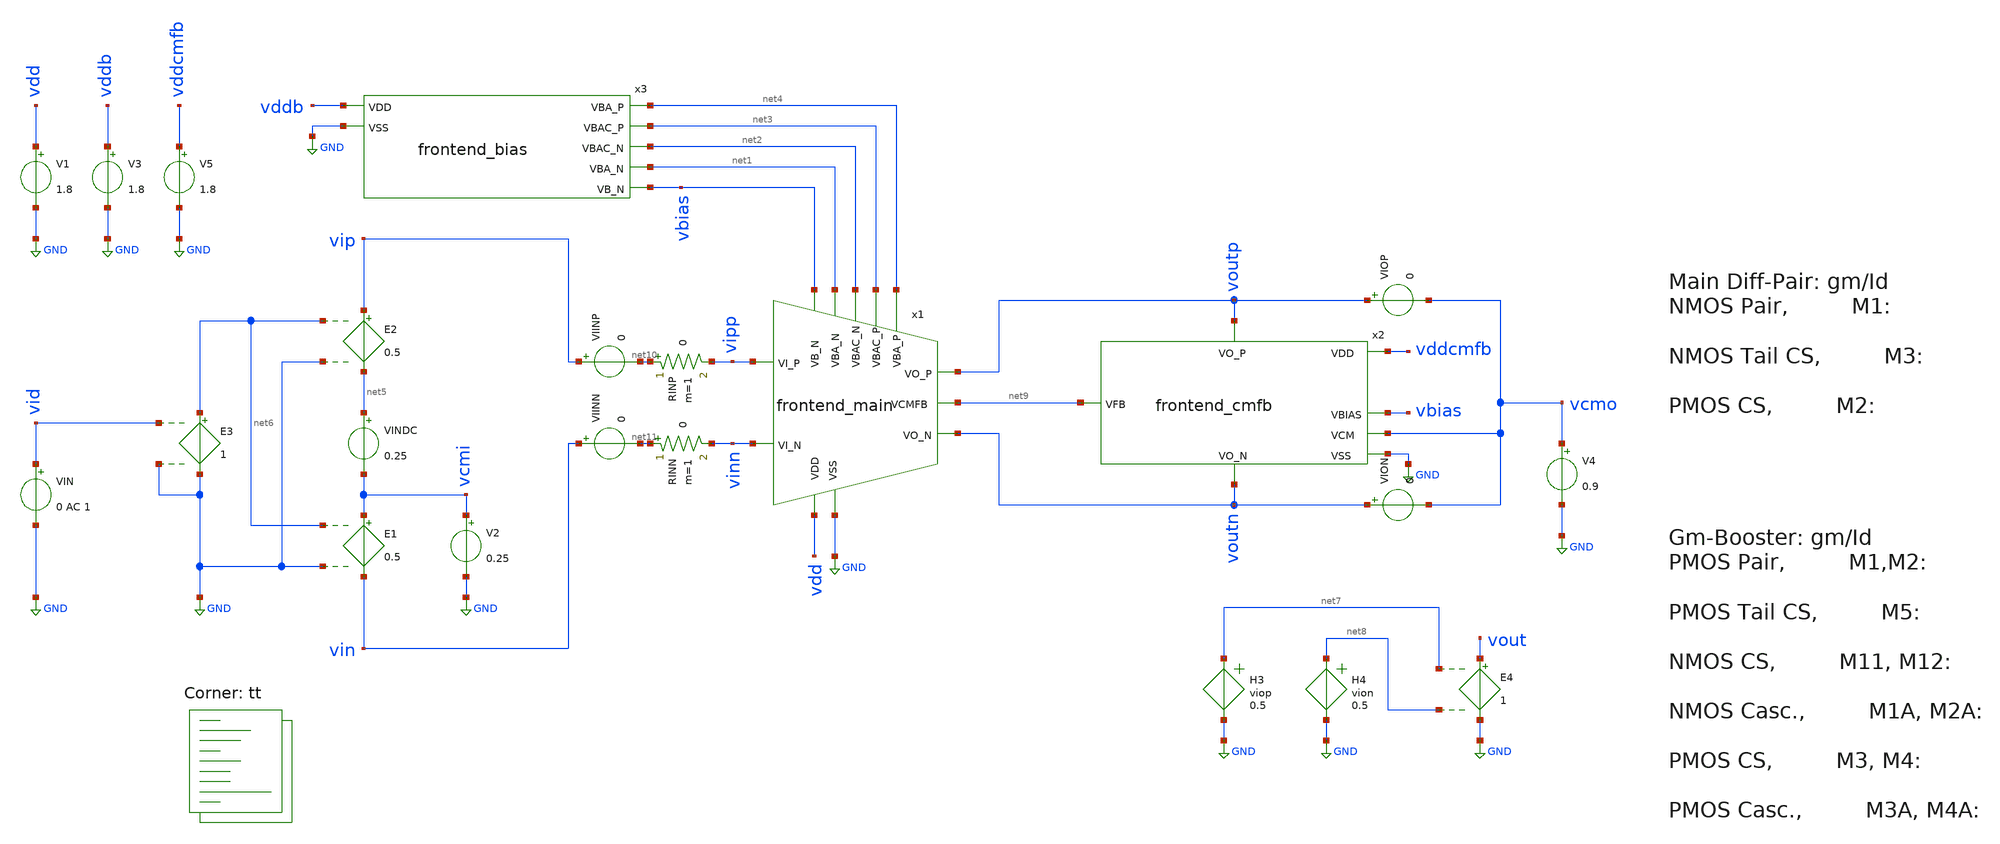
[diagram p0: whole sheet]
** sch_path: circuit-level/xschem/frontend/frontend_tb_dc.sch
**.subckt frontend_tb_dc
V1 vdd GND 1.8
V2 vcmi GND 0.25
E1 vcmi vin net6 GND 0.5
E2 vip net5 net6 GND 0.5
VIN vid GND 0 AC 1
VINDC net5 vcmi 0.25
x2 vddcmfb net9 voutp voutn vbias vcmo GND frontend_cmfb
x3 vddb net4 net3 net2 net1 vbias GND frontend_bias
V3 vddb GND 1.8
V4 vcmo GND 0.9
E3 net6 GND vid GND 1
VIOP voutp vcmo 0
VION voutn vcmo 0
H3 net7 GND viop 0.5
H4 net8 GND vion 0.5
E4 vout GND net7 net8 1
x1 vdd net9 net1 net2 net3 net4 voutp voutn vipp vinn vbias GND frontend_main
V5 vddcmfb GND 1.8
RINP net10 vipp 0 m=1
RINN net11 vinn 0 m=1
VIINP vip net10 0
VIINN vin net11 0
**** begin user architecture code
.lib $::SKYWATER_MODELS/sky130.lib.spice tt


.options savecurrents
.control
save all

let f_sig = 32
let f_min = 0.1
let f_max = 128
let tper_sig = 1/f_sig
let tfr_sig = tper_sig/2
alter @VIN[SIN] = [ 0 0.01 $&f_sig 0 0 0 ]
alter @VIN[DC] = 0.0

let tstep = 0.01/f_sig
let tstop = 500/f_sig
let tstart = 2500*tstep

set fndc = /foss/designs/frontend/frontend_dc.txt
set fntran = /foss/designs/frontend/frontend_tran.txt
set fnspec = /foss/designs/frontend/frontend_spec.txt
set fnhd = /foss/designs/frontend/frontend_hd.txt
set fnnoise = /foss/designs/frontend/frontend_noise.txt
set wr_singlescale
set wr_vecnames
option numdgt=5


** Main Simulations
	alter @VINDC[DC] = 0
	dc VIN -500m 500m 31m
	ac dec 1000 0.1 1e7
	alter @VINDC[DC] = 0.25
	tran $&tstep $&tstop $&tstart
	alter @VINDC[DC] = 0
	noise v(vout) VIN dec 100 0.01 100k 1
	noise v(vout) VIN dec 10 0.01 128
	alter @rinp[resistance] = 10G
	alter @rinn[resistance] = 10G
	alter @VIN[SIN] = [ 0 0.1 128 0 0 0 ]
	alter @VINDC[DC] = 0
	tran $&tstep $&tstop $&tstart

	setplot noise1
	let acgain = onoise_spectrum/inoise_spectrum

	let mdiffpair_gmb_in = sqrt(4)*onoise.m.x1.x1.xm1a.msky130_fd_pr__pfet_01v8/acgain
	let mload_gmb_in = sqrt(4)*onoise.m.x1.x1.xm3a.msky130_fd_pr__nfet_01v8/acgain
	let mload_in = sqrt(2)*onoise.m.x1.xm2a.msky130_fd_pr__pfet_01v8_lvt/acgain
	let mdiffpair_in = sqrt(2)*onoise.m.x1.xm1a.msky130_fd_pr__nfet_01v8/acgain
	let mtail_in = onoise.m.x1.xm3a.msky130_fd_pr__nfet_01v8/acgain
	*let m1b_in = onoise.m.xm1b.msky130_fd_pr__nfet_01v8/acgain

	*let m2a_in = onoise.m.xm2a.msky130_fd_pr__pfet_01v8_lvt/acgain
	*let m2b_in = onoise.m.xm2b.msky130_fd_pr__pfet_01v8_lvt/acgain

	*let m3a_in = onoise.m.xm3a.msky130_fd_pr__nfet_01v8/acgain
	*let m3b_in = onoise.m.xm3b.msky130_fd_pr__nfet_01v8/acgain

	let rs_in = sqrt(onoise_r.x1.rs1^2+onoise_r.x1.rs2^2)/acgain

	*plot inoise_spectrum m1a_in m2a_in m3a_in rs_in

	*plot m2a_in m2b_in
	plot inoise_spectrum rs_in mdiffpair_gmb_in mload_gmb_in mload_in mdiffpair_in ylog xlog
	wrdata $fnnoise inoise_spectrum rs_in mdiffpair_gmb_in mload_gmb_in mload_in mdiffpair_in

	setplot ac1
	let A = v(vout)/v(vin)
	plot vdb(A) 180/PI*phase(A)

	let i_in_p = viinp#branch
	let i_in_n = viinn#branch
	let zin = abs((v(vip)-v(vin))/(2*(i_in_p-i_in_n)))
	meas ac zin_fmax find zin when frequency=128

	plot vdb(zin)

	setplot dc1
	let vid = v(vid)
	let iod = (viop#branch-vion#branch)
	let gm  = abs(iod/vid)
	plot iod
	plot gm 0
	wrdata $fndc iod gm

	setplot tran1
	let vid = v(vid)
	let iod = (viop#branch-vion#branch)

	meas tran iod_max max iod
	meas tran vid_max max vid
	let gm = iod_max/vid_max
	plot iod

	*plot gm
	wrdata $fntran iod

	** FFT

	linearize iod
	set specwindow=hanning
	fft iod
	setplot sp5

	let N = length(iod)
	let fres = frequency[n-1]/n
	let fmin_idx = ceil(const.f_min/fres)
	let fmax_idx = ceil(const.f_max/fres)

	let iod_spec = mag(iod)
	let iod_spec_slice = iod_spec[fmin_idx,fmax_idx]
	let freq = frequency[fmin_idx,fmax_idx]
	meas sp iod_max max iod_spec_slice
	let iod_spec_db = 20*log10(iod_spec_slice/iod_max)
	plot iod_spec_db vs freq

	** Calc HD2, HD3
	let sig_idx = ceil(const.f_sig/fres)
	let hd2_idx = 2*sig_idx
	let hd3_idx = 3*sig_idx
	let sig_pwr = iod_spec[sig_idx-1]^2+iod_spec[sig_idx]^2+iod_spec[sig_idx+1]^2
	let hd2_pwr = iod_spec[hd2_idx-1]^2+iod_spec[hd2_idx]^2+iod_spec[hd2_idx+1]^2
	let hd3_pwr = iod_spec[hd3_idx-1]^2+iod_spec[hd3_idx]^2+iod_spec[hd3_idx+1]^2
	let hd2 = sqrt(hd2_pwr/sig_pwr)
	let hd3 = sqrt(hd3_pwr/sig_pwr)
	let hd2_dB = 20*log10(hd2)
	let hd3_dB = 20*log10(hd3)
	setscale freq
	wrdata $fnspec iod_spec_db
	*wrdata $fnhd hd3[0] hd3_db[0] hd2[0] hd2_db[0] fres n

	** Input Impedance
	setplot tran4
	let vrinn = v(vin,vinn)
	let vrinp = v(vip,vipp)

	plot vrinp vrinn 25m

alter @VIN[DC] = 0
op
let gmId1 = @m.x1.x1.xm1a.msky130_fd_pr__pfet_01v8[gm]/@m.x1.x1.xm1a.msky130_fd_pr__pfet_01v8[id]
let gmId5 = @m.x1.x1.xm2a.msky130_fd_pr__pfet_01v8[gm]/@m.x1.x1.xm2a.msky130_fd_pr__pfet_01v8[id]
let gmId11 = @m.x1.x1.xm3a.msky130_fd_pr__nfet_01v8[gm]/@m.x1.x1.xm3a.msky130_fd_pr__nfet_01v8[id]
let gmId1a = @m.x1.x1.xm4a.msky130_fd_pr__nfet_01v8[gm]/@m.x1.x1.xm4a.msky130_fd_pr__nfet_01v8[id]
let gmId3 = @m.x1.x1.xm5a.msky130_fd_pr__pfet_01v8[gm]/@m.x1.x1.xm5a.msky130_fd_pr__pfet_01v8[id]
let gmId3a = @m.x1.x1.xm5a.msky130_fd_pr__pfet_01v8[gm]/@m.x1.x1.xm6a.msky130_fd_pr__pfet_01v8[id]

let gmId1_main = @m.x1.xm1a.msky130_fd_pr__nfet_01v8[gm]/@m.x1.xm1a.msky130_fd_pr__nfet_01v8[id]
let gmId_tail = @m.x1.xm3a.msky130_fd_pr__nfet_01v8[gm]/@m.x1.xm3a.msky130_fd_pr__nfet_01v8[id]
let gmId_load =
+ @m.x1.xm2a.msky130_fd_pr__pfet_01v8_lvt[gm]/@m.x1.xm2a.msky130_fd_pr__pfet_01v8_lvt[id]
remzerovec
write frontend_tb_dc.raw
.endc

**** end user architecture code
**.ends
.GLOBAL GND
.end
